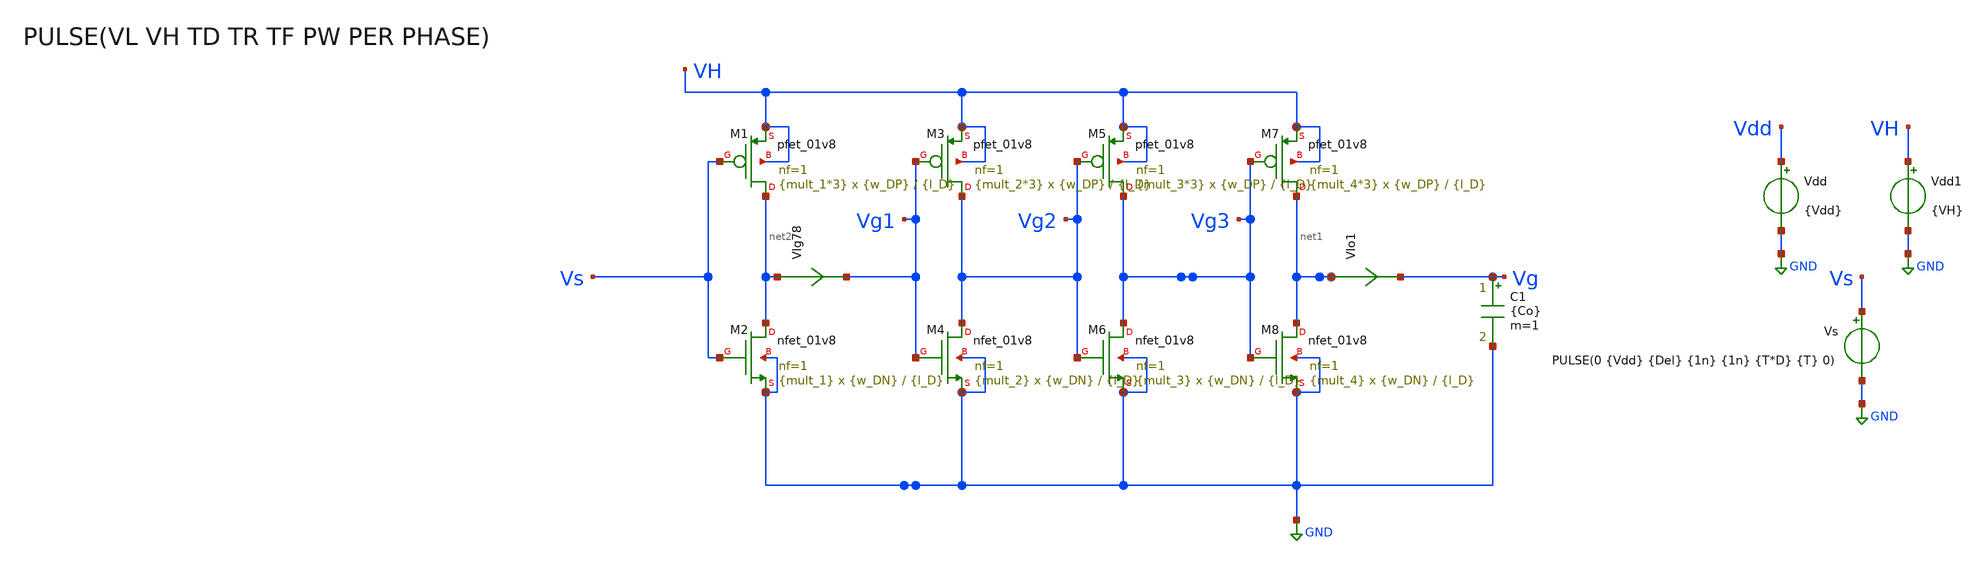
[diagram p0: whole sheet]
** sch_path: xschem/GD/TB_GateDriver_woSimbol.sch
**.subckt TB_GateDriver_woSimbol
Vdd Vdd GND {Vdd}
Vs Vs GND PULSE(0 {Vdd} {Del} {1n} {1n} {T*D} {T} 0)
Vdd1 VH GND {VH}
C1 Vg GND {Co} m=1
VIo1 net1 Vg 0
.save i(vio1)
VIg78 net2 Vg1 0
.save i(vig78)
XM2 net2 Vs GND GND sky130_fd_pr__nfet_01v8 L={l_D} W={w_DN} nf=1 ad='int((nf+1)/2) * W/nf * 0.29' as='int((nf+2)/2) * W/nf * 0.29'
+ pd='2*int((nf+1)/2) * (W/nf + 0.29)' ps='2*int((nf+2)/2) * (W/nf + 0.29)' nrd='0.29 / W' nrs='0.29 / W'
+ sa=0 sb=0 sd=0 mult={mult_1} m={mult_1}
XM1 net2 Vs VH VH sky130_fd_pr__pfet_01v8 L={l_D} W={w_DP} nf=1 ad='int((nf+1)/2) * W/nf * 0.29' as='int((nf+2)/2) * W/nf * 0.29'
+ pd='2*int((nf+1)/2) * (W/nf + 0.29)' ps='2*int((nf+2)/2) * (W/nf + 0.29)' nrd='0.29 / W' nrs='0.29 / W'
+ sa=0 sb=0 sd=0 mult={mult_1*3} m={mult_1*3}
XM3 Vg2 Vg1 VH VH sky130_fd_pr__pfet_01v8 L={l_D} W={w_DP} nf=1 ad='int((nf+1)/2) * W/nf * 0.29' as='int((nf+2)/2) * W/nf * 0.29'
+ pd='2*int((nf+1)/2) * (W/nf + 0.29)' ps='2*int((nf+2)/2) * (W/nf + 0.29)' nrd='0.29 / W' nrs='0.29 / W'
+ sa=0 sb=0 sd=0 mult={mult_2*3} m={mult_2*3}
XM4 Vg2 Vg1 GND GND sky130_fd_pr__nfet_01v8 L={l_D} W={w_DN} nf=1 ad='int((nf+1)/2) * W/nf * 0.29' as='int((nf+2)/2) * W/nf * 0.29'
+ pd='2*int((nf+1)/2) * (W/nf + 0.29)' ps='2*int((nf+2)/2) * (W/nf + 0.29)' nrd='0.29 / W' nrs='0.29 / W'
+ sa=0 sb=0 sd=0 mult={mult_2} m={mult_2}
XM5 Vg3 Vg2 VH VH sky130_fd_pr__pfet_01v8 L={l_D} W={w_DP} nf=1 ad='int((nf+1)/2) * W/nf * 0.29' as='int((nf+2)/2) * W/nf * 0.29'
+ pd='2*int((nf+1)/2) * (W/nf + 0.29)' ps='2*int((nf+2)/2) * (W/nf + 0.29)' nrd='0.29 / W' nrs='0.29 / W'
+ sa=0 sb=0 sd=0 mult={mult_3*3} m={mult_3*3}
XM6 Vg3 Vg2 GND GND sky130_fd_pr__nfet_01v8 L={l_D} W={w_DN} nf=1 ad='int((nf+1)/2) * W/nf * 0.29' as='int((nf+2)/2) * W/nf * 0.29'
+ pd='2*int((nf+1)/2) * (W/nf + 0.29)' ps='2*int((nf+2)/2) * (W/nf + 0.29)' nrd='0.29 / W' nrs='0.29 / W'
+ sa=0 sb=0 sd=0 mult={mult_3} m={mult_3}
XM7 net1 Vg3 VH VH sky130_fd_pr__pfet_01v8 L={l_D} W={w_DP} nf=1 ad='int((nf+1)/2) * W/nf * 0.29' as='int((nf+2)/2) * W/nf * 0.29'
+ pd='2*int((nf+1)/2) * (W/nf + 0.29)' ps='2*int((nf+2)/2) * (W/nf + 0.29)' nrd='0.29 / W' nrs='0.29 / W'
+ sa=0 sb=0 sd=0 mult={mult_4*3} m={mult_4*3}
XM8 net1 Vg3 GND GND sky130_fd_pr__nfet_01v8 L={l_D} W={w_DN} nf=1 ad='int((nf+1)/2) * W/nf * 0.29' as='int((nf+2)/2) * W/nf * 0.29'
+ pd='2*int((nf+1)/2) * (W/nf + 0.29)' ps='2*int((nf+2)/2) * (W/nf + 0.29)' nrd='0.29 / W' nrs='0.29 / W'
+ sa=0 sb=0 sd=0 mult={mult_4} m={mult_4}
**** begin user architecture code


.param Vdd = 1.8
.param VH = 1.8

.param Co = 63p

.param D = 0.5
*.param T = 1u
.param T = 0.1u
.param TR = 10n
.param TF = 10n
*.param TdR = 0.1u
.param TdR = 1n
*.param TdF = 0.1u
.param TdF = 1n
.param Del = 0.05u
.param temp = 27






.save all
.control
reset
set color0 = white
tran 1n 1u

plot v(Vs)
plot v(Vg)
plot i(VIo1)

*meas TRAN td_off_M1 TRIG v(Vg_M1) VAL=0.33 RISE=1 TARG VsdM1 VAL=0.33 RISE=1
*meas TRAN td_on_M1 TRIG v(Vg_M1) VAL=2.97 FALL=1 TARG VsdM1 VAL=2.97 FALL=1
*meas TRAN td_on_M2 TRIG v(Vg_M2) VAL=0.33 RISE=1 TARG VdsM2 VAL=2.97 FALL=1
*meas TRAN td_off_M2 TRIG v(Vg_M2) VAL=2.97 FALL=1 TARG VdsM2 VAL=0.33 RISE=1
*let TdR = td_off_M1 - td_on_M2
*let TdF = td_on_M1 - td_off_M2
*print TdR TdF
.endc

.end




.param temp=27

.param mult_1 = 1
.param mult_2 = 10
.param mult_3 = 30
.param mult_4 = 250

.param l_D = 0.15
.param w_DP = 0.42
.param w_DN = 0.42





.lib /opt/pdks/sky130A/libs.tech/ngspice/sky130.lib.spice tt
*.lib /opt/pdks/sky130A/libs.tech/ngspice/sky130.lib.spice ss
*.lib /opt/pdks/sky130A/libs.tech/ngspice/sky130.lib.spice ff
*.lib /opt/pdks/sky130A/libs.tech/ngspice/sky130.lib.spice sf
*.lib /opt/pdks/sky130A/libs.tech/ngspice/sky130.lib.spice fs

**** end user architecture code
**.ends
.GLOBAL GND
.end
